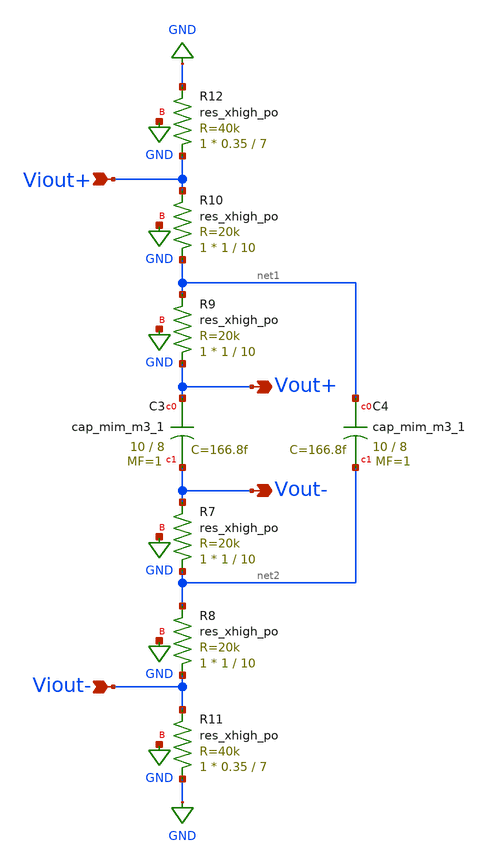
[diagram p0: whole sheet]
** sch_path: simulation/filter/filter_lvs.sch
**.subckt filter_lvs Vout+ Vout- Viout+ Viout-
*.opin Vout+
*.opin Vout-
*.ipin Viout+
*.ipin Viout-
XC3 Vout+ Vout- sky130_fd_pr__cap_mim_m3_1 W=10 L=8 MF=1 m=1
XC4 net1 net2 sky130_fd_pr__cap_mim_m3_1 W=10 L=8 MF=1 m=1
XR7 net2 Vout- GND sky130_fd_pr__res_xhigh_po W=1 L=10 mult=1 m=1
XR8 Viout- net2 GND sky130_fd_pr__res_xhigh_po W=1 L=10 mult=1 m=1
XR9 Vout+ net1 GND sky130_fd_pr__res_xhigh_po W=1 L=10 mult=1 m=1
XR10 net1 Viout+ GND sky130_fd_pr__res_xhigh_po W=1 L=10 mult=1 m=1
XR11 GND Viout- GND sky130_fd_pr__res_xhigh_po W=0.35 L=7 mult=1 m=1
XR12 Viout+ GND GND sky130_fd_pr__res_xhigh_po W=0.35 L=7 mult=1 m=1
**.ends
.GLOBAL GND
.end
